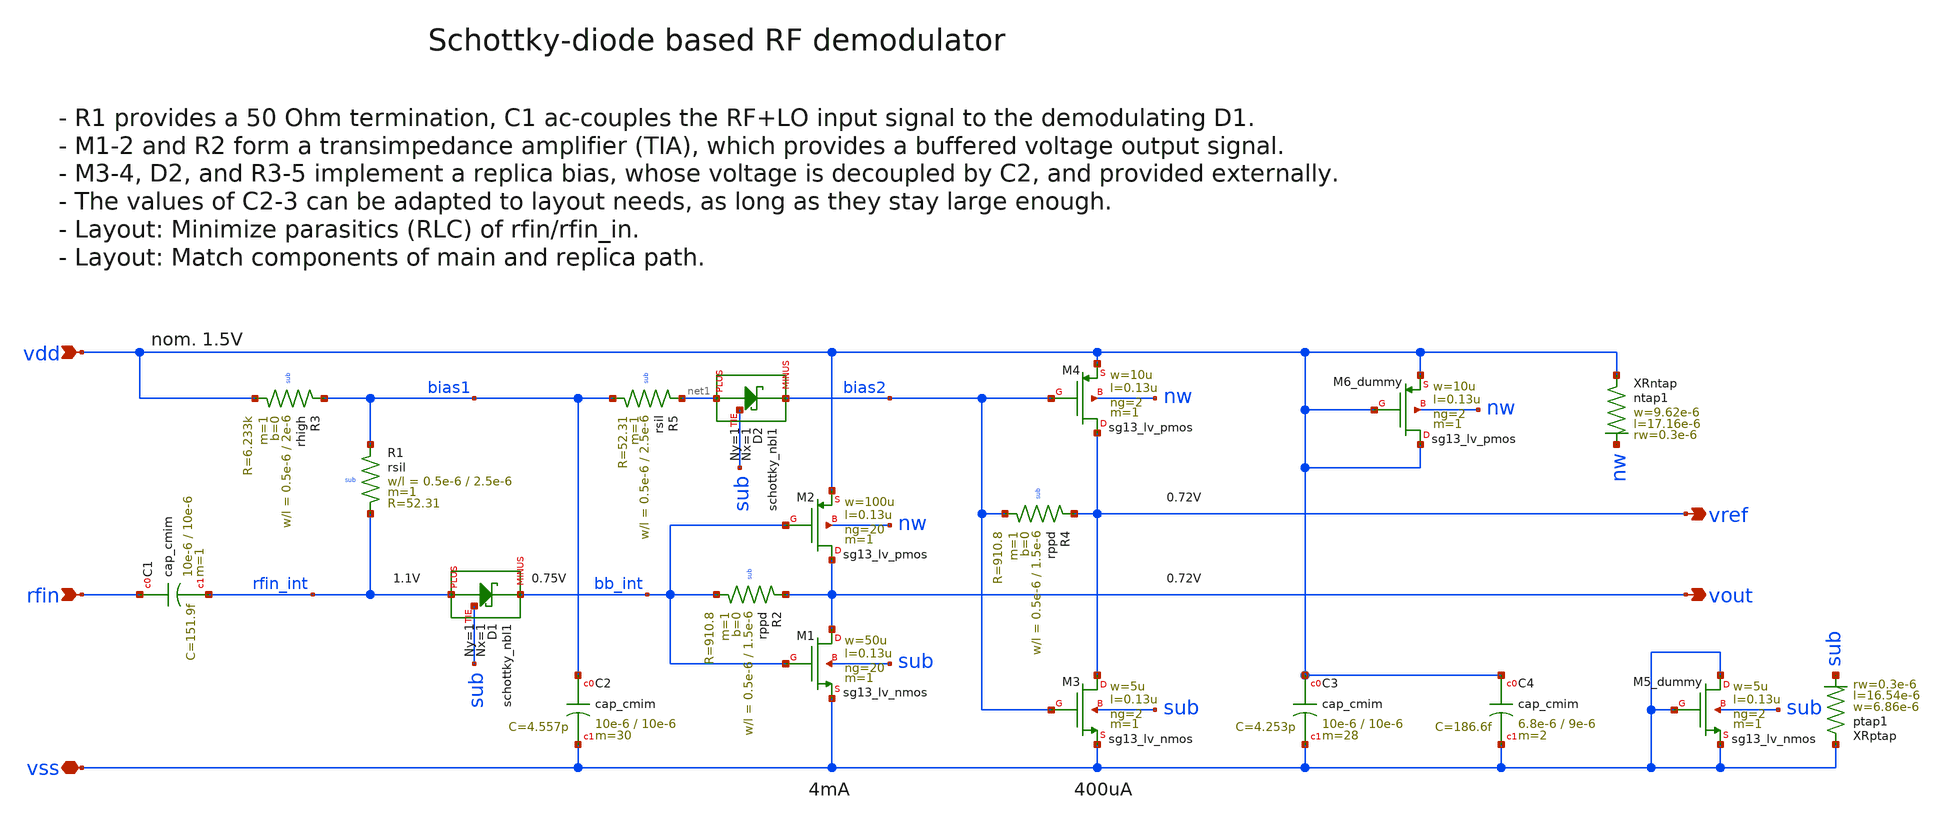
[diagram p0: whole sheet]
** sch_path: schematic/sparx160_powdet_sbd_woLVSopen.sch
* (c) 2026 Harald Pretl ICD@JKU
**.subckt sparx160_powdet_sbd_woLVSopen rfin vout vss vdd vref
*.ipin rfin
*.opin vout
*.iopin vss
*.ipin vdd
*.opin vref
XR1 bias1 rfin_int sub rsil w=0.5e-6 l=2.5e-6 m=1 mm_ok=1
XD1 rfin_int bb_int sub schottky_nbl1 Nx=1 Ny=1
XC2 bias1 vss cap_cmim w=10e-6 l=10e-6 m=30 mm_ok=1
XM2 vout bb_int vdd nw sg13_lv_pmos w=100u l=0.13u ng=20 m=1 mm_ok=1
XM1 vout bb_int vss sub sg13_lv_nmos w=50u l=0.13u ng=20 m=1 mm_ok=1
XR2 vout bb_int sub rppd w=0.5e-6 l=1.5e-6 m=1 b=0 mm_ok=1
XM4 vref bias2 vdd nw sg13_lv_pmos w=10u l=0.13u ng=2 m=1 mm_ok=1
XM3 vref bias2 vss sub sg13_lv_nmos w=5u l=0.13u ng=2 m=1 mm_ok=1
XC3 vdd vss cap_cmim w=10e-6 l=10e-6 m=28 mm_ok=1
XD2 net1 bias2 sub schottky_nbl1 Nx=1 Ny=1
XR3 bias1 vdd sub rhigh w=0.5e-6 l=2e-6 m=1 b=0 mm_ok=1
XR4 vref bias2 sub rppd w=0.5e-6 l=1.5e-6 m=1 b=0 mm_ok=1
XR5 net1 bias1 sub rsil w=0.5e-6 l=2.5e-6 m=1 mm_ok=1
XM5_dummy vss vss vss sub sg13_lv_nmos w=5u l=0.13u ng=2 m=1 mm_ok=1
XM6_dummy vdd vdd vdd nw sg13_lv_pmos w=10u l=0.13u ng=2 m=1 mm_ok=1
XC1 rfin rfin_int cap_cmim w=10e-6 l=10e-6 m=1 mm_ok=1
XRntap vdd nw ntap1 R=4.353 w=9.62e-6 l=17.16e-6 rw=0.3e-6
XRptap vss sub ptap1 R=4.998 w=6.86e-6 l=16.54e-6 rw=0.3e-6
XC4 vdd vss cap_cmim w=6.8e-6 l=9e-6 m=2 mm_ok=1
**.ends
.end
